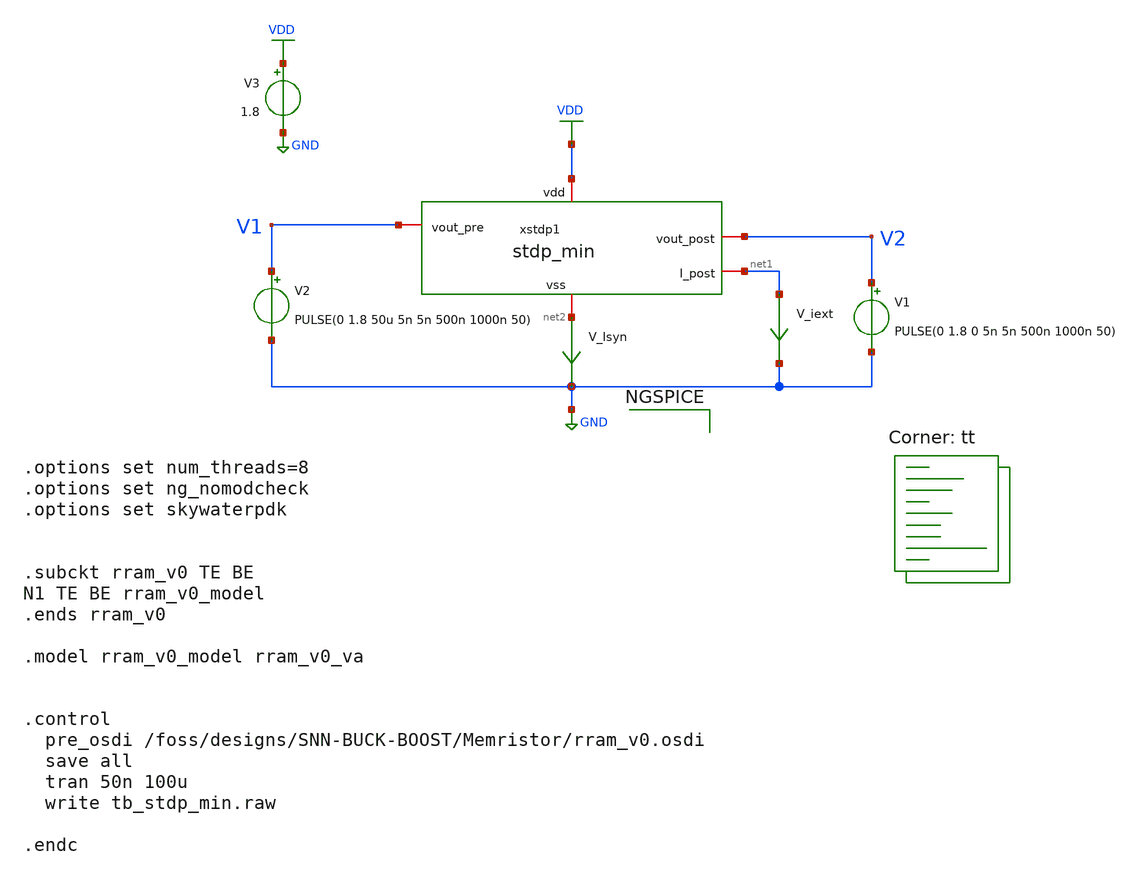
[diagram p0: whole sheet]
** sch_path: Synapse/tb_stdp_min.sch
**.subckt tb_stdp_min
V_iext net1 GND 0
.save i(v_iext)
V3 VDD GND 1.8
xstdp1 VDD net2 V1 V2 net1 stdp_min
V1 V2 GND PULSE(0 1.8 0 5n 5n 500n 1000n 50)
V2 V1 GND PULSE(0 1.8 50u 5n 5n 500n 1000n 50)
V_Isyn net2 GND 0
.save i(v_isyn)
**** begin user architecture code



.options set num_threads=8
.options set ng_nomodcheck
.options set skywaterpdk


.subckt rram_v0 TE BE
N1 TE BE rram_v0_model
.ends rram_v0

.model rram_v0_model rram_v0_va


.control
  pre_osdi /foss/designs/SNN-BUCK-BOOST/Memristor/rram_v0.osdi
  save all
  tran 50n 100u
  write tb_stdp_min.raw

.endc



.lib $::SKYWATER_MODELS/sky130.lib.spice tt
**** end user architecture code
**.ends

* expanding   symbol:  stdp_min.sym # of pins=5
** sym_path: Synapse/stdp_min.sym
** sch_path: Synapse/stdp_min.sch
.subckt stdp_min vdd vss vout_pre vout_post I_post
*.iopin vdd
*.iopin vss
*.iopin vout_post
*.iopin vout_pre
*.iopin I_post
XM3 be vout_post vss vss sky130_fd_pr__nfet_01v8 L=0.15 W=0.5 nf=1 ad='int((nf+1)/2) * W/nf * 0.29' as='int((nf+2)/2) * W/nf * 0.29'
+ pd='2*int((nf+1)/2) * (W/nf + 0.29)' ps='2*int((nf+2)/2) * (W/nf + 0.29)' nrd='0.29 / W' nrs='0.29 / W'
+ sa=0 sb=0 sd=0 mult=1 m=1
XM4 net1 vout_pre vss vss sky130_fd_pr__nfet_01v8 L=0.15 W=0.5 nf=1 ad='int((nf+1)/2) * W/nf * 0.29'
+ as='int((nf+2)/2) * W/nf * 0.29' pd='2*int((nf+1)/2) * (W/nf + 0.29)' ps='2*int((nf+2)/2) * (W/nf + 0.29)'
+ nrd='0.29 / W' nrs='0.29 / W' sa=0 sb=0 sd=0 mult=1 m=1
XR2 be te rram_v0
XM14 net3 net2 vdd vdd sky130_fd_pr__pfet_01v8 L=0.15 W=0.5 nf=1 ad='int((nf+1)/2) * W/nf * 0.29' as='int((nf+2)/2) * W/nf * 0.29'
+ pd='2*int((nf+1)/2) * (W/nf + 0.29)' ps='2*int((nf+2)/2) * (W/nf + 0.29)' nrd='0.29 / W' nrs='0.29 / W'
+ sa=0 sb=0 sd=0 mult=1 m=1
XM15 net2 net2 vdd vdd sky130_fd_pr__pfet_01v8 L=0.15 W=1 nf=1 ad='int((nf+1)/2) * W/nf * 0.29' as='int((nf+2)/2) * W/nf * 0.29'
+ pd='2*int((nf+1)/2) * (W/nf + 0.29)' ps='2*int((nf+2)/2) * (W/nf + 0.29)' nrd='0.29 / W' nrs='0.29 / W'
+ sa=0 sb=0 sd=0 mult=1 m=1
**** begin user architecture code


.save v(te) v(be) i(vmr)


**** end user architecture code
Vmr te net1 0
.save i(vmr)
XM5 n_vout_pre vout_pre vdd vdd sky130_fd_pr__pfet_01v8 L=0.15 W=1 nf=1 ad='int((nf+1)/2) * W/nf * 0.29'
+ as='int((nf+2)/2) * W/nf * 0.29' pd='2*int((nf+1)/2) * (W/nf + 0.29)' ps='2*int((nf+2)/2) * (W/nf + 0.29)'
+ nrd='0.29 / W' nrs='0.29 / W' sa=0 sb=0 sd=0 mult=1 m=1
XM7 n_vout_pre vout_pre vss vss sky130_fd_pr__nfet_01v8 L=0.15 W=1 nf=1 ad='int((nf+1)/2) * W/nf * 0.29'
+ as='int((nf+2)/2) * W/nf * 0.29' pd='2*int((nf+1)/2) * (W/nf + 0.29)' ps='2*int((nf+2)/2) * (W/nf + 0.29)'
+ nrd='0.29 / W' nrs='0.29 / W' sa=0 sb=0 sd=0 mult=1 m=1
XM8 n_vout_post vout_post vdd vdd sky130_fd_pr__pfet_01v8 L=0.15 W=1 nf=1 ad='int((nf+1)/2) * W/nf * 0.29'
+ as='int((nf+2)/2) * W/nf * 0.29' pd='2*int((nf+1)/2) * (W/nf + 0.29)' ps='2*int((nf+2)/2) * (W/nf + 0.29)'
+ nrd='0.29 / W' nrs='0.29 / W' sa=0 sb=0 sd=0 mult=1 m=1
XM9 n_vout_post vout_post vss vss sky130_fd_pr__nfet_01v8 L=0.15 W=1 nf=1 ad='int((nf+1)/2) * W/nf * 0.29'
+ as='int((nf+2)/2) * W/nf * 0.29' pd='2*int((nf+1)/2) * (W/nf + 0.29)' ps='2*int((nf+2)/2) * (W/nf + 0.29)'
+ nrd='0.29 / W' nrs='0.29 / W' sa=0 sb=0 sd=0 mult=1 m=1
XM1 net1 n_vout_post net2 vdd sky130_fd_pr__pfet_01v8 L=0.15 W=1 nf=1 ad='int((nf+1)/2) * W/nf * 0.29'
+ as='int((nf+2)/2) * W/nf * 0.29' pd='2*int((nf+1)/2) * (W/nf + 0.29)' ps='2*int((nf+2)/2) * (W/nf + 0.29)'
+ nrd='0.29 / W' nrs='0.29 / W' sa=0 sb=0 sd=0 mult=1 m=1
XM2 be n_vout_pre net2 vdd sky130_fd_pr__pfet_01v8 L=0.15 W=1 nf=1 ad='int((nf+1)/2) * W/nf * 0.29' as='int((nf+2)/2) * W/nf * 0.29'
+ pd='2*int((nf+1)/2) * (W/nf + 0.29)' ps='2*int((nf+2)/2) * (W/nf + 0.29)' nrd='0.29 / W' nrs='0.29 / W'
+ sa=0 sb=0 sd=0 mult=1 m=1
XM6 I_post net2 net3 vdd sky130_fd_pr__pfet_01v8 L=0.15 W=0.5 nf=1 ad='int((nf+1)/2) * W/nf * 0.29' as='int((nf+2)/2) * W/nf * 0.29'
+ pd='2*int((nf+1)/2) * (W/nf + 0.29)' ps='2*int((nf+2)/2) * (W/nf + 0.29)' nrd='0.29 / W' nrs='0.29 / W'
+ sa=0 sb=0 sd=0 mult=1 m=1
.ends

.GLOBAL GND
.GLOBAL VDD
.end
